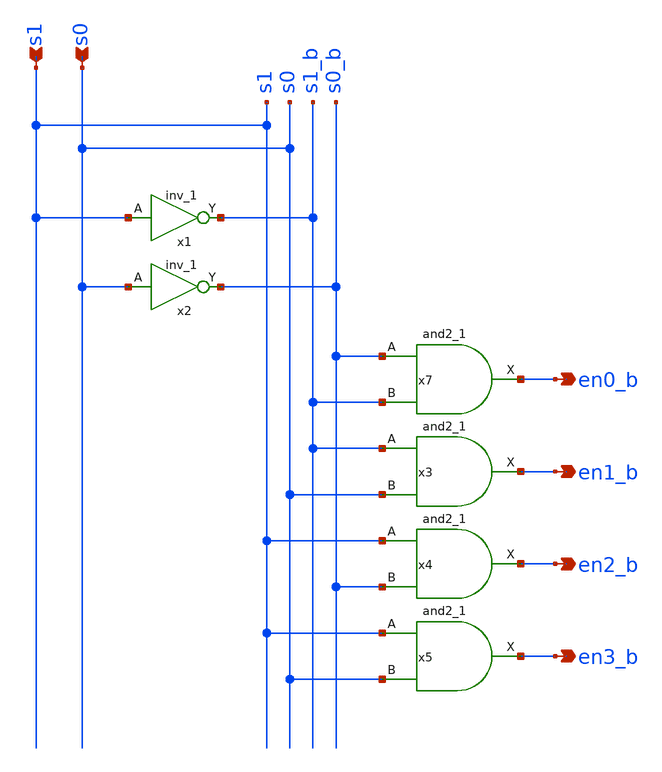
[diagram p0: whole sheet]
** sch_path: analog_mux/verification/2to4_decoder.sch
**.subckt 2to4_decoder s0 en0_b s1 en1_b en2_b en3_b
*.ipin s0
*.opin en0_b
*.ipin s1
*.opin en1_b
*.opin en2_b
*.opin en3_b
x1 s1 VGND VNB VPB VPWR s1_b sky130_fd_sc_hd__inv_1
x2 s0 VGND VNB VPB VPWR s0_b sky130_fd_sc_hd__inv_1
x7 s0_b s1_b VGND VNB VPB VPWR en0_b sky130_fd_sc_hd__and2_1
x3 s1_b s0 VGND VNB VPB VPWR en1_b sky130_fd_sc_hd__and2_1
x4 s1 s0_b VGND VNB VPB VPWR en2_b sky130_fd_sc_hd__and2_1
x5 s1 s0 VGND VNB VPB VPWR en3_b sky130_fd_sc_hd__and2_1
**.ends
.end
